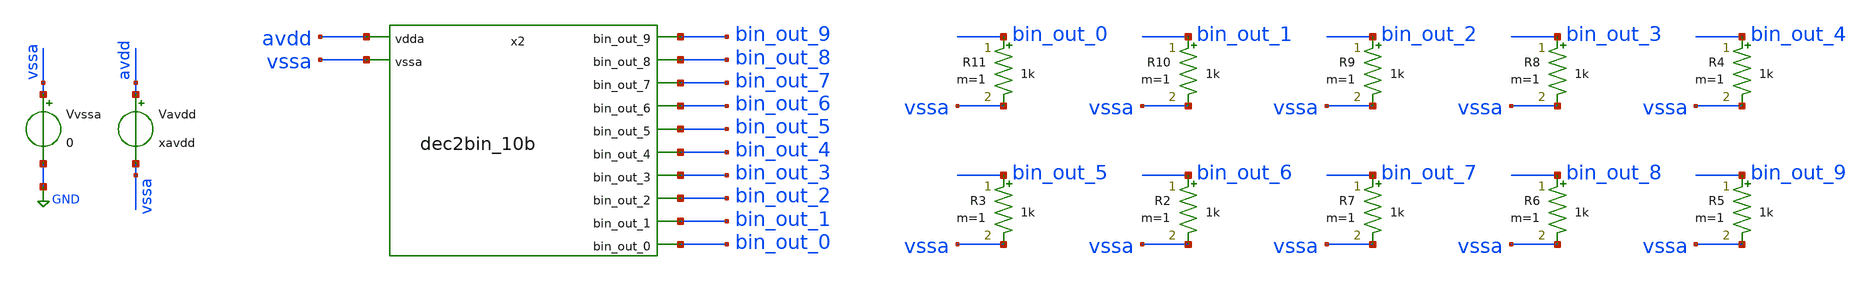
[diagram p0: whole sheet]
** sch_path: Passing_variables_to_vloga_files/tb_dec2bin_10b_sweep.sch
**.subckt tb_dec2bin_10b_sweep
x2 bin_out_9 bin_out_8 bin_out_7 bin_out_6 bin_out_5 bin_out_4 bin_out_3 bin_out_2 bin_out_1
+ bin_out_0 avdd vssa dec2bin_10b dec_code=dec_code_var
Vavdd avdd vssa xavdd
Vvssa vssa GND 0
R2 bin_out_6 vssa 1k m=1
R3 bin_out_5 vssa 1k m=1
R4 bin_out_4 vssa 1k m=1
R5 bin_out_9 vssa 1k m=1
R6 bin_out_8 vssa 1k m=1
R7 bin_out_7 vssa 1k m=1
R8 bin_out_3 vssa 1k m=1
R9 bin_out_2 vssa 1k m=1
R10 bin_out_1 vssa 1k m=1
R11 bin_out_0 vssa 1k m=1
**** begin user architecture code

** opencircuitdesign pdks install
*.lib $::SKYWATER_MODELS/sky130.lib.spice tt
.lib /home/slice/pdk/SW130/share/pdk/sky130A/libs.tech/combined/sky130.lib.spice tt
*.lib /home/slice/pdk/SW130/share/pdk/sky130A/libs.tech/combined/sky130.lib.spice ss
*.lib /home/slice/pdk/SW130/share/pdk/sky130A/libs.tech/combined/sky130.lib.spice ff
*.lib /home/slice/pdk/SW130/share/pdk/sky130A/libs.tech/combined/sky130.lib.spice sf
*.lib /home/slice/pdk/SW130/share/pdk/sky130A/libs.tech/combined/sky130.lib.spice fs

.include /home/slice/pdk/SW130/share/pdk/sky130A/libs.ref/sky130_fd_sc_hd/spice/sky130_fd_sc_hd.spice

* Parameters
.param xavdd = 3.3
.param xdvdd = 1.8
.param xvcm = xavdd/2
.param xibias = 100n
.param xCload = 100f
.param xRload = 100Meg
.param xtsim = 5u
.param xvin_se = 0.5m
.param dec_code_var = 0
*.csparam xdec_code_var = 'dec_code_var'
.csparam xtsim_var = 'xtsim'

.temp 27

.model dec2bin_10b dec2bin_10b

  .control

  pre_osdi dec2bin_10b.osdi
  *save all
  save v(vout) v(vcm) v(vinp) v(vinn) v(avdd) v(dvdd) v(bin_out_9) v(bin_out_8) v(bin_out_7)
+ v(bin_out_6) v(bin_out_5) v(bin_out_4) v(bin_out_3) v(bin_out_2) v(bin_out_1) v(bin_out_0)
  save i(Vavdd)
  *.option savecurrents
  echo $&xtsim_var
  echo $&xdec_code_var

  let xdec_code_var = 0

   repeat 16                  ; loop start
   alterparam dec_code_var = $&xdec_code_var;        ; alter the decimal code
   reset

** 1. TRAN ANALYSIS **

  tran 10n $&xtsim_var
  remzerovec

  *set filetype=ascii
  write tb_ina_pa_tran_data.raw
  set appendwrite

** 2. MEASURES **
    echo "$&xdec_code_var" >> code_measures.txt
    echo -- >> code_measures.txt
    meas TRAN out0_ave AVG v(bin_out_0) from=0 to= $&xtsim_var
    meas TRAN out1_ave AVG v(bin_out_1) from=0 to= $&xtsim_var
    meas TRAN out2_ave AVG v(bin_out_2) from=0 to= $&xtsim_var
    meas TRAN out3_ave AVG v(bin_out_3) from=0 to= $&xtsim_var
    meas TRAN out4_ave AVG v(bin_out_4) from=0 to= $&xtsim_var
    meas TRAN out5_ave AVG v(bin_out_5) from=0 to= $&xtsim_var
    echo "$&out0_ave" >> code_measures.txt
    echo "$&out1_ave" >> code_measures.txt
    echo "$&out2_ave" >> code_measures.txt
    echo "$&out3_ave" >> code_measures.txt
    echo "$&out4_ave" >> code_measures.txt
    echo "$&out5_ave" >> code_measures.txt
    echo -- >> code_measures.txt

   let xdec_code_var = xdec_code_var + 1;
   end


  setplot

quit 0
.endc









**** end user architecture code
**.ends

* expanding   symbol:  dec2bin_10b.sym # of pins=12
** sym_path: Passing_variables_to_vloga_files/dec2bin_10b.sym
** sch_path: Passing_variables_to_vloga_files/dec2bin_10b.sch
.subckt dec2bin_10b bin_out_9 bin_out_8 bin_out_7 bin_out_6 bin_out_5 bin_out_4 bin_out_3 bin_out_2
+ bin_out_1 bin_out_0 vdda vssa  dec_code=0
*.ipin vdda
*.opin bin_out_9
*.opin bin_out_8
*.opin bin_out_7
*.opin bin_out_6
*.opin bin_out_5
*.opin bin_out_4
*.opin bin_out_3
*.opin bin_out_2
*.opin bin_out_1
*.opin bin_out_0
*.ipin vssa
* noconn bin_out_9
* noconn bin_out_8
* noconn bin_out_7
* noconn bin_out_6
* noconn bin_out_5
* noconn bin_out_4
* noconn bin_out_3
* noconn bin_out_2
* noconn bin_out_1
* noconn bin_out_0
* noconn vdda
* noconn vssa
**** begin user architecture code
N1 bin_out_9 bin_out_8 bin_out_7 bin_out_6 bin_out_5 bin_out_4 bin_out_3 bin_out_2 bin_out_1
+ bin_out_0 vdda vssa dec2bin_10b dec_code = dec_code
**** end user architecture code
.ends

.GLOBAL GND
.end
